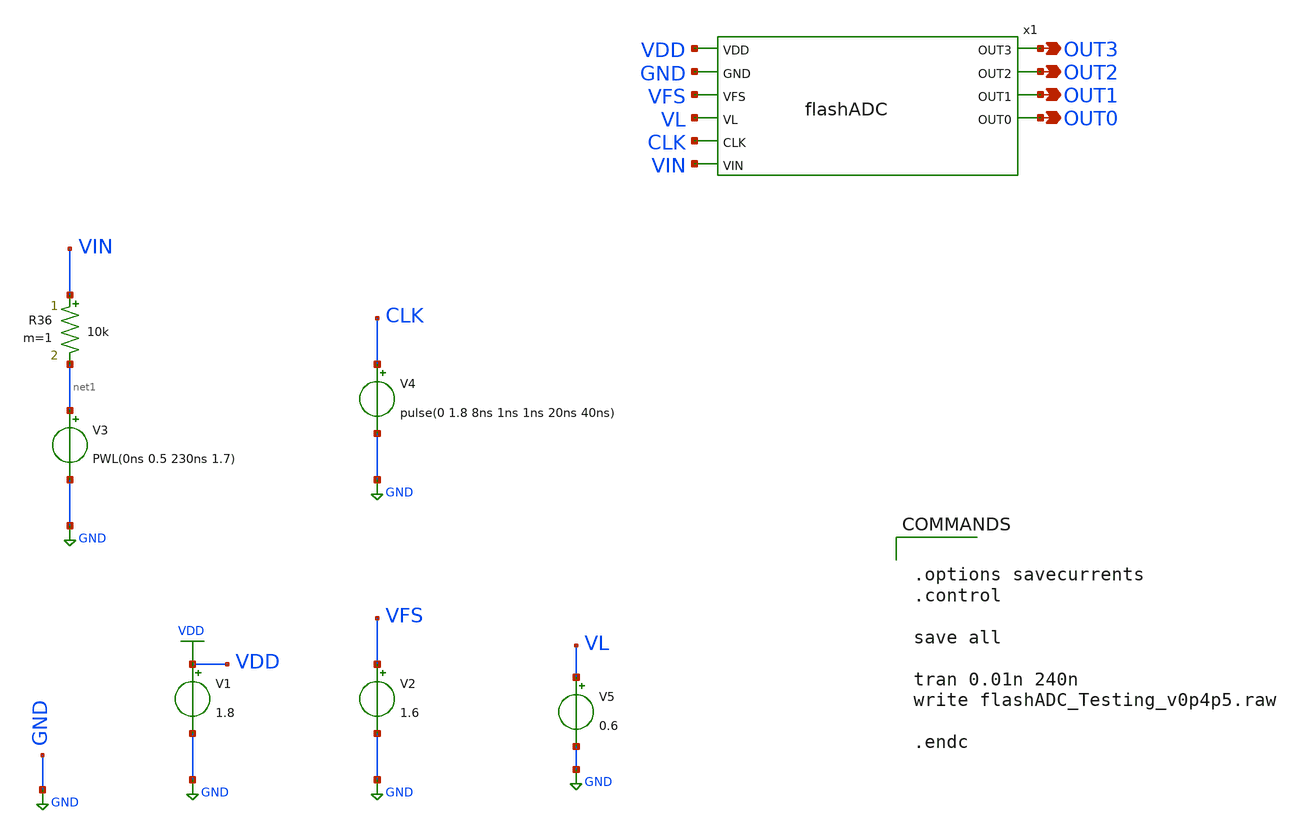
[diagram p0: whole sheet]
** sch_path: flashADC/xschem/flashADC_Testing_v0p4p5.sch
.lib $::SKYWATER_MODELS/sky130.lib.spice tt
.include $::SKYWATER_STDCELLS/sky130_fd_sc_hd.spice

**.subckt flashADC_Testing_v0p4p5 OUT3 OUT2 OUT1 OUT0
*.opin OUT3
*.opin OUT2
*.opin OUT1
*.opin OUT0
V4 CLK GND pulse(0 1.8 8ns 1ns 1ns 20ns 40ns)
V1 VDD GND 1.8
V2 VFS GND 1.6
V5 VL GND 0.6
x1 VDD GND VIN CLK OUT3 VFS OUT2 VL OUT1 OUT0 flashADC
V3 net1 GND PWL(0ns 0.5 230ns 1.7)
R36 VIN net1 10k m=1
**** begin user architecture code


.options savecurrents
.control

save all

tran 0.01n 240n
write flashADC_Testing_v0p4p5.raw

.endc


**** end user architecture code
**.ends
.GLOBAL GND
.GLOBAL VDD
.end
